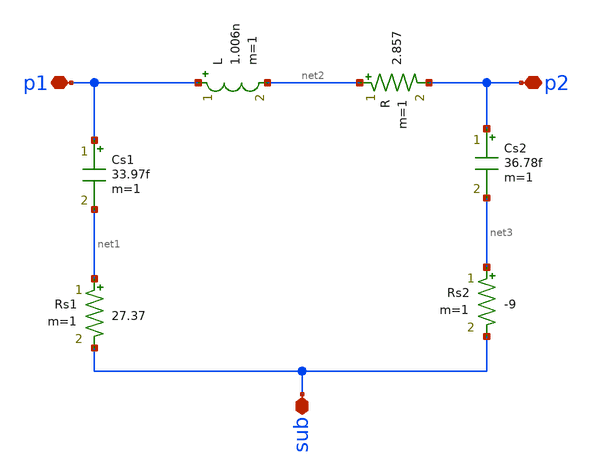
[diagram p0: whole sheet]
** sch_path: examples/sq_1nH_2.5GHz/xschem/l0.sch
**.subckt l0 sub p1 p2
*.iopin sub
*.iopin p1
*.iopin p2
R net2 p2 2.857 m=1
L p1 net2 1.006n m=1
Rs1 net1 sub 27.37 m=1
Cs1 p1 net1 33.97f m=1
Cs2 p2 net3 36.78f m=1
Rs2 net3 sub -9 m=1
**.ends
.end
